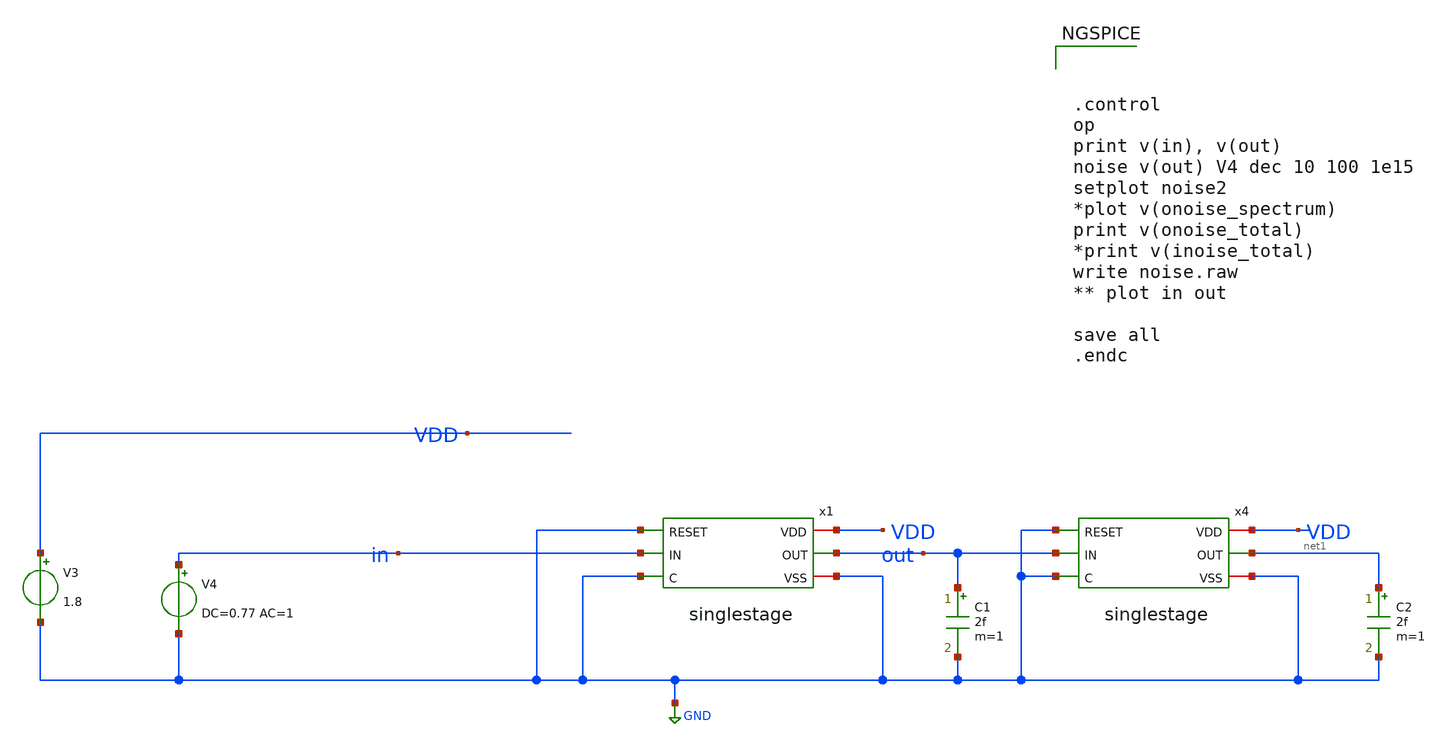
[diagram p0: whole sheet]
** sch_path: design/brpuf_noise.sch
**.subckt brpuf_noise
V3 VDD GND 1.8
V4 in GND DC=0.77 AC=1
C2 net1 GND 2f m=1
x1 GND VDD GND out in GND singlestage
x4 GND VDD GND net1 out GND singlestage
C1 out GND 2f m=1
**** begin user architecture code

** opencircuitdesign pdks install
.lib $::SKYWATER_MODELS/sky130.lib.spice tt_mm
.include $::SKYWATER_STDCELLS/sky130_fd_sc_hd.spice





.control
op
print v(in), v(out)
noise v(out) V4 dec 10 100 1e15
setplot noise2
*plot v(onoise_spectrum)
print v(onoise_total)
*print v(inoise_total)
write noise.raw
** plot in out

save all
.endc


**** end user architecture code
**.ends

* expanding   symbol:  design/singlestage.sym # of pins=6
** sym_path: design/singlestage.sym
** sch_path: design/singlestage.sch
.subckt singlestage RESET VDD VSS OUT IN C
*.ipin IN
*.ipin C
*.ipin RESET
*.iopin VSS
*.iopin VDD
*.opin OUT
x1 RESET net1 VSS VSS VDD VDD net3 sky130_fd_sc_hd__nor2_1
x2 RESET net2 VSS VSS VDD VDD net4 sky130_fd_sc_hd__nor2_1
x3 net6 VSS net1 VDD IN net5 net2 demux2-1
x4 net6 VSS net3 VDD OUT net5 net4 mux2-1
x5 net5 VSS VSS VDD VDD net6 sky130_fd_sc_hd__inv_1
XM1 net1 net6 VDD VDD sky130_fd_pr__pfet_01v8_hvt L=0.15 W=1 nf=1 ad='int((nf+1)/2) * W/nf * 0.29' as='int((nf+2)/2) * W/nf * 0.29'
+ pd='2*int((nf+1)/2) * (W/nf + 0.29)' ps='2*int((nf+2)/2) * (W/nf + 0.29)' nrd='0.29 / W' nrs='0.29 / W'
+ sa=0 sb=0 sd=0 mult=1 m=1
XM2 net2 net5 VDD VDD sky130_fd_pr__pfet_01v8_hvt L=0.15 W=1 nf=1 ad='int((nf+1)/2) * W/nf * 0.29' as='int((nf+2)/2) * W/nf * 0.29'
+ pd='2*int((nf+1)/2) * (W/nf + 0.29)' ps='2*int((nf+2)/2) * (W/nf + 0.29)' nrd='0.29 / W' nrs='0.29 / W'
+ sa=0 sb=0 sd=0 mult=1 m=1
x6 C VSS VSS VDD VDD net5 sky130_fd_sc_hd__inv_1
.ends


* expanding   symbol:  demux2-1.sym # of pins=7
** sym_path: xiaolin/demux2-1.sym
** sch_path: xiaolin/demux2-1.sch
.subckt demux2-1 S VSS OUT1 VDD IN Sbar OUT2
*.ipin Sbar
*.ipin S
*.iopin VSS
*.iopin VDD
*.opin OUT1
*.opin OUT2
*.ipin IN
XM2 IN S OUT1 VSS sky130_fd_pr__nfet_01v8 L=0.15 W=0.65 nf=1 ad='int((nf+1)/2) * W/nf * 0.29' as='int((nf+2)/2) * W/nf * 0.29'
+ pd='2*int((nf+1)/2) * (W/nf + 0.29)' ps='2*int((nf+2)/2) * (W/nf + 0.29)' nrd='0.29 / W' nrs='0.29 / W'
+ sa=0 sb=0 sd=0 mult=1 m=1
XM1 IN Sbar OUT2 VSS sky130_fd_pr__nfet_01v8 L=0.15 W=0.65 nf=1 ad='int((nf+1)/2) * W/nf * 0.29' as='int((nf+2)/2) * W/nf * 0.29'
+ pd='2*int((nf+1)/2) * (W/nf + 0.29)' ps='2*int((nf+2)/2) * (W/nf + 0.29)' nrd='0.29 / W' nrs='0.29 / W'
+ sa=0 sb=0 sd=0 mult=1 m=1
XM3 IN S OUT2 VDD sky130_fd_pr__pfet_01v8_hvt L=0.15 W=1 nf=1 ad='int((nf+1)/2) * W/nf * 0.29' as='int((nf+2)/2) * W/nf * 0.29'
+ pd='2*int((nf+1)/2) * (W/nf + 0.29)' ps='2*int((nf+2)/2) * (W/nf + 0.29)' nrd='0.29 / W' nrs='0.29 / W'
+ sa=0 sb=0 sd=0 mult=1 m=1
XM4 IN Sbar OUT1 VDD sky130_fd_pr__pfet_01v8_hvt L=0.15 W=1 nf=1 ad='int((nf+1)/2) * W/nf * 0.29' as='int((nf+2)/2) * W/nf * 0.29'
+ pd='2*int((nf+1)/2) * (W/nf + 0.29)' ps='2*int((nf+2)/2) * (W/nf + 0.29)' nrd='0.29 / W' nrs='0.29 / W'
+ sa=0 sb=0 sd=0 mult=1 m=1
XM5 IN S OUT2 VDD sky130_fd_pr__pfet_01v8_hvt L=0.15 W=1 nf=1 ad='int((nf+1)/2) * W/nf * 0.29' as='int((nf+2)/2) * W/nf * 0.29'
+ pd='2*int((nf+1)/2) * (W/nf + 0.29)' ps='2*int((nf+2)/2) * (W/nf + 0.29)' nrd='0.29 / W' nrs='0.29 / W'
+ sa=0 sb=0 sd=0 mult=1 m=1
.ends


* expanding   symbol:  mux2-1.sym # of pins=7
** sym_path: design/mux2-1.sym
** sch_path: design/mux2-1.sch
.subckt mux2-1 S VSS IN1 VDD OUT Sbar IN2
*.ipin IN1
*.ipin IN2
*.ipin Sbar
*.ipin S
*.opin OUT
*.iopin VSS
*.iopin VDD
XM2 IN1 S OUT VSS sky130_fd_pr__nfet_01v8 L=0.15 W=0.65 nf=1 ad='int((nf+1)/2) * W/nf * 0.29' as='int((nf+2)/2) * W/nf * 0.29'
+ pd='2*int((nf+1)/2) * (W/nf + 0.29)' ps='2*int((nf+2)/2) * (W/nf + 0.29)' nrd='0.29 / W' nrs='0.29 / W'
+ sa=0 sb=0 sd=0 mult=1 m=1
XM1 IN2 Sbar OUT VSS sky130_fd_pr__nfet_01v8 L=0.15 W=0.65 nf=1 ad='int((nf+1)/2) * W/nf * 0.29' as='int((nf+2)/2) * W/nf * 0.29'
+ pd='2*int((nf+1)/2) * (W/nf + 0.29)' ps='2*int((nf+2)/2) * (W/nf + 0.29)' nrd='0.29 / W' nrs='0.29 / W'
+ sa=0 sb=0 sd=0 mult=1 m=1
XM4 IN1 Sbar OUT VDD sky130_fd_pr__pfet_01v8_hvt L=0.15 W=1 nf=1 ad='int((nf+1)/2) * W/nf * 0.29' as='int((nf+2)/2) * W/nf * 0.29'
+ pd='2*int((nf+1)/2) * (W/nf + 0.29)' ps='2*int((nf+2)/2) * (W/nf + 0.29)' nrd='0.29 / W' nrs='0.29 / W'
+ sa=0 sb=0 sd=0 mult=1 m=1
XM5 IN2 S OUT VDD sky130_fd_pr__pfet_01v8_hvt L=0.15 W=1 nf=1 ad='int((nf+1)/2) * W/nf * 0.29' as='int((nf+2)/2) * W/nf * 0.29'
+ pd='2*int((nf+1)/2) * (W/nf + 0.29)' ps='2*int((nf+2)/2) * (W/nf + 0.29)' nrd='0.29 / W' nrs='0.29 / W'
+ sa=0 sb=0 sd=0 mult=1 m=1
.ends

.GLOBAL GND
.end
